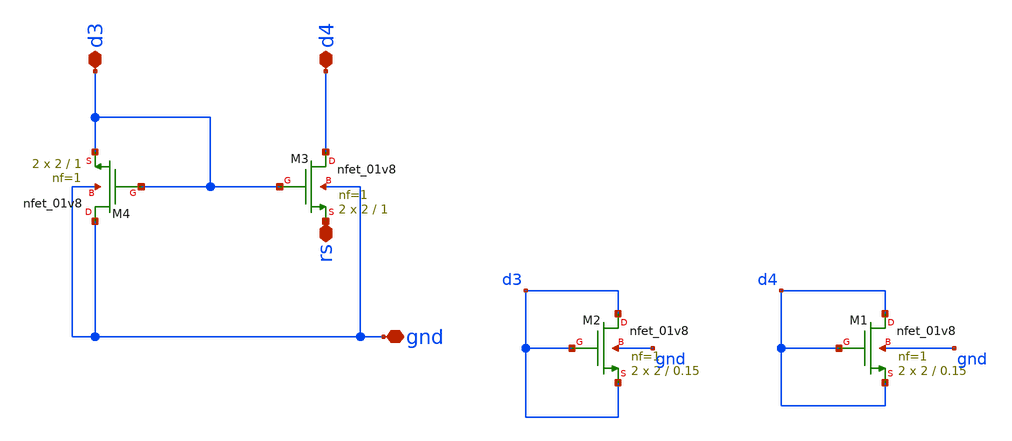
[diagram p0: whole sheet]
** sch_path: opamp/mag/nmoscs.sch
**.subckt nmoscs rs gnd d4 d3
*.iopin rs
*.iopin gnd
*.iopin d4
*.iopin d3
XM3 d4 d3 rs gnd sky130_fd_pr__nfet_01v8 L=1 W=2 nf=1 ad='int((nf+1)/2) * W/nf * 0.29' as='int((nf+2)/2) * W/nf * 0.29'
+ pd='2*int((nf+1)/2) * (W/nf + 0.29)' ps='2*int((nf+2)/2) * (W/nf + 0.29)' nrd='0.29 / W' nrs='0.29 / W'
+ sa=0 sb=0 sd=0 mult=2 m=2
XM4 gnd d3 d3 gnd sky130_fd_pr__nfet_01v8 L=1 W=2 nf=1 ad='int((nf+1)/2) * W/nf * 0.29' as='int((nf+2)/2) * W/nf * 0.29'
+ pd='2*int((nf+1)/2) * (W/nf + 0.29)' ps='2*int((nf+2)/2) * (W/nf + 0.29)' nrd='0.29 / W' nrs='0.29 / W'
+ sa=0 sb=0 sd=0 mult=2 m=2
XM2 d3 d3 d3 gnd sky130_fd_pr__nfet_01v8 L=0.15 W=2 nf=1 ad='int((nf+1)/2) * W/nf * 0.29' as='int((nf+2)/2) * W/nf * 0.29'
+ pd='2*int((nf+1)/2) * (W/nf + 0.29)' ps='2*int((nf+2)/2) * (W/nf + 0.29)' nrd='0.29 / W' nrs='0.29 / W'
+ sa=0 sb=0 sd=0 mult=2 m=2
XM1 d4 d4 d4 gnd sky130_fd_pr__nfet_01v8 L=0.15 W=2 nf=1 ad='int((nf+1)/2) * W/nf * 0.29' as='int((nf+2)/2) * W/nf * 0.29'
+ pd='2*int((nf+1)/2) * (W/nf + 0.29)' ps='2*int((nf+2)/2) * (W/nf + 0.29)' nrd='0.29 / W' nrs='0.29 / W'
+ sa=0 sb=0 sd=0 mult=2 m=2
**.ends
.end
